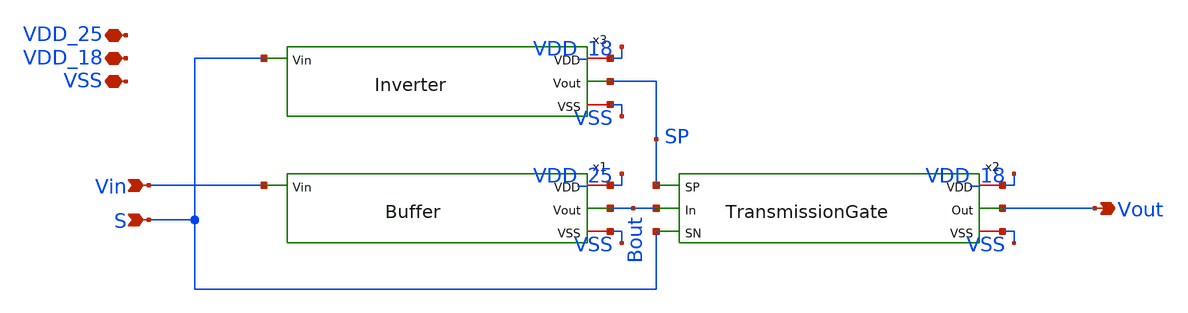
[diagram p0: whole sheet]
** sch_path: xschem/1LineSelectInput.sch
**.subckt 1LineSelectInput VDD_18 VSS Vin Vout S VDD_25
*.iopin VDD_18
*.iopin VSS
*.ipin Vin
*.opin Vout
*.ipin S
*.iopin VDD_25
x1 VDD_25 Vin Bout VSS Buffer
x2 SP VDD_18 Vout Bout VSS S TransmissionGate
x3 VDD_18 S SP VSS Inverter
**.ends

* expanding   symbol:  Buffer.sym # of pins=4
** sym_path: xschem/Buffer.sym
** sch_path: xschem/Buffer.sch
.subckt Buffer VDD Vin Vout VSS
*.iopin VDD
*.iopin VSS
*.ipin Vin
*.opin Vout
x1 VDD Vin net1 VSS Inverter
x2 VDD net1 Vout VSS Inverter
.ends


* expanding   symbol:  TransmissionGate.sym # of pins=6
** sym_path: xschem/TransmissionGate.sym
** sch_path: xschem/TransmissionGate.sch
.subckt TransmissionGate SP VDD Out In VSS SN
*.opin Out
*.ipin In
*.ipin SP
*.iopin VDD
*.iopin VSS
*.ipin SN
XM1 In SN Out VSS sky130_fd_pr__nfet_g5v0d10v5 L=0.5 W=0.75 nf=1 ad='int((nf+1)/2) * W/nf * 0.29' as='int((nf+2)/2) * W/nf * 0.29'
+ pd='2*int((nf+1)/2) * (W/nf + 0.29)' ps='2*int((nf+2)/2) * (W/nf + 0.29)' nrd='0.29 / W' nrs='0.29 / W'
+ sa=0 sb=0 sd=0 mult=1 m=1
XM2 In SP Out VDD sky130_fd_pr__pfet_g5v0d10v5 L=0.5 W=1.5 nf=1 ad='int((nf+1)/2) * W/nf * 0.29' as='int((nf+2)/2) * W/nf * 0.29'
+ pd='2*int((nf+1)/2) * (W/nf + 0.29)' ps='2*int((nf+2)/2) * (W/nf + 0.29)' nrd='0.29 / W' nrs='0.29 / W'
+ sa=0 sb=0 sd=0 mult=1 m=1
.ends


* expanding   symbol:  Inverter.sym # of pins=4
** sym_path: xschem/Inverter.sym
** sch_path: xschem/Inverter.sch
.subckt Inverter VDD Vin Vout VSS
*.ipin Vin
*.iopin VDD
*.iopin VSS
*.opin Vout
XM1 Vout Vin VSS VSS sky130_fd_pr__nfet_g5v0d10v5 L=0.5 W=0.75 nf=1 ad='int((nf+1)/2) * W/nf * 0.29'
+ as='int((nf+2)/2) * W/nf * 0.29' pd='2*int((nf+1)/2) * (W/nf + 0.29)' ps='2*int((nf+2)/2) * (W/nf + 0.29)'
+ nrd='0.29 / W' nrs='0.29 / W' sa=0 sb=0 sd=0 mult=1 m=1
XM2 Vout Vin VDD VDD sky130_fd_pr__pfet_g5v0d10v5 L=0.5 W=1.5 nf=1 ad='int((nf+1)/2) * W/nf * 0.29' as='int((nf+2)/2) * W/nf * 0.29'
+ pd='2*int((nf+1)/2) * (W/nf + 0.29)' ps='2*int((nf+2)/2) * (W/nf + 0.29)' nrd='0.29 / W' nrs='0.29 / W'
+ sa=0 sb=0 sd=0 mult=1 m=1
.ends

.end
